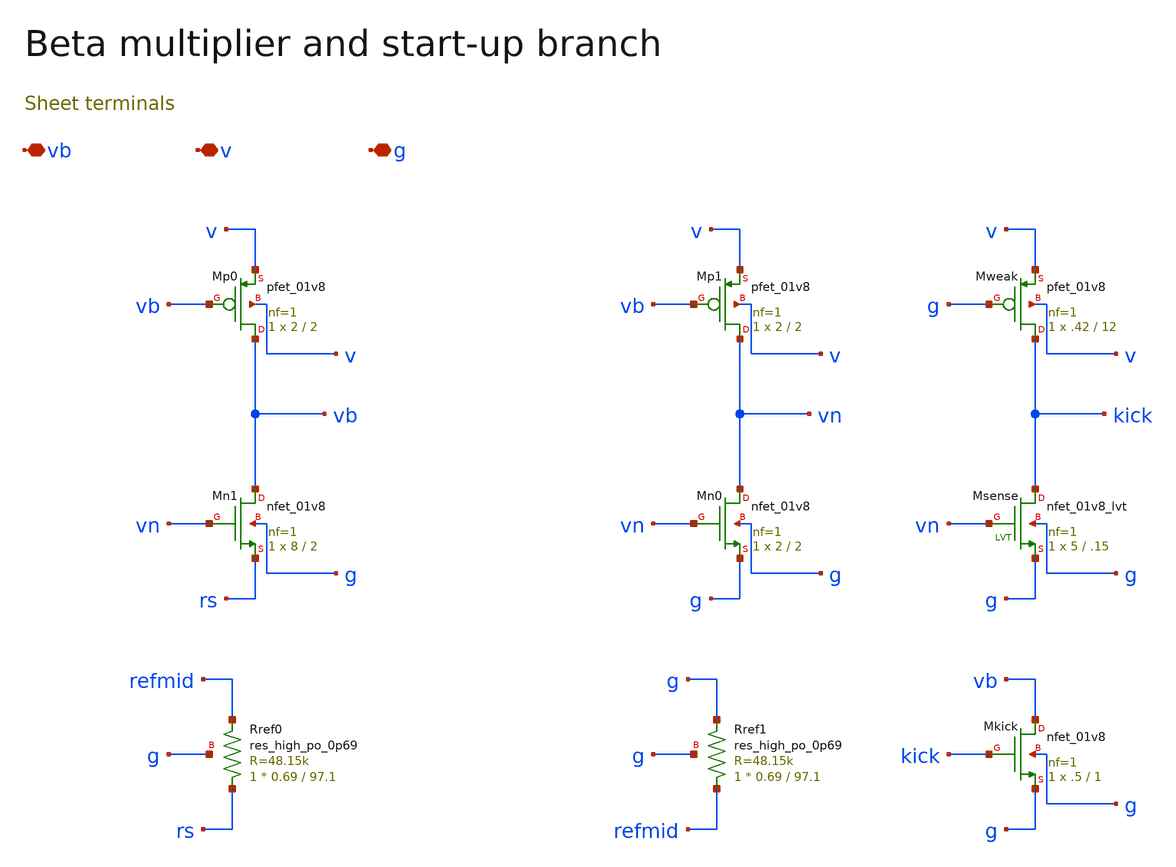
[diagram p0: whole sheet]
** sch_path: review/xschem/beta_ref.sch
**.subckt beta_ref vb v g
*.iopin vb
*.iopin v
*.iopin g
XMp0 vb vb v v sky130_fd_pr__pfet_01v8 L=2 W=2 nf=1 ad='int((nf+1)/2) * W/nf * 0.29' as='int((nf+2)/2) * W/nf * 0.29'
+ pd='2*int((nf+1)/2) * (W/nf + 0.29)' ps='2*int((nf+2)/2) * (W/nf + 0.29)' nrd='0.29 / W' nrs='0.29 / W'
+ sa=0 sb=0 sd=0 mult=1 m=1
XMn0 vn vn g g sky130_fd_pr__nfet_01v8 L=2 W=2 nf=1 ad='int((1 + 1)/2) * 2 / 1 * 0.29' as='int((1 + 2)/2) * 2 / 1 * 0.29'
+ pd='2*int((1 + 1)/2) * (2 / 1 + 0.29)' ps='2*int((1 + 2)/2) * (2 / 1 + 0.29)' nrd='0.29 / 2 ' nrs='0.29 / 2 '
+ sa=0 sb=0 sd=0 mult=1 m=1
XMp1 vn vb v v sky130_fd_pr__pfet_01v8 L=2 W=2 nf=1 ad='int((nf+1)/2) * W/nf * 0.29' as='int((nf+2)/2) * W/nf * 0.29'
+ pd='2*int((nf+1)/2) * (W/nf + 0.29)' ps='2*int((nf+2)/2) * (W/nf + 0.29)' nrd='0.29 / W' nrs='0.29 / W'
+ sa=0 sb=0 sd=0 mult=1 m=1
XMn1 vb vn rs g sky130_fd_pr__nfet_01v8 L=2 W=8 nf=1 ad='int((1 + 1)/2) * 8 / 1 * 0.29' as='int((1 + 2)/2) * 8 / 1 * 0.29'
+ pd='2*int((1 + 1)/2) * (8 / 1 + 0.29)' ps='2*int((1 + 2)/2) * (8 / 1 + 0.29)' nrd='0.29 / 8 ' nrs='0.29 / 8 '
+ sa=0 sb=0 sd=0 mult=1 m=1
XRref0 rs refmid g sky130_fd_pr__res_high_po_0p69 L=97.1 mult=1 m=1
XRref1 refmid g g sky130_fd_pr__res_high_po_0p69 L=97.1 mult=1 m=1
XMweak kick g v v sky130_fd_pr__pfet_01v8 L=12 W=.42 nf=1 ad='int((nf+1)/2) * W/nf * 0.29' as='int((nf+2)/2) * W/nf * 0.29'
+ pd='2*int((nf+1)/2) * (W/nf + 0.29)' ps='2*int((nf+2)/2) * (W/nf + 0.29)' nrd='0.29 / W' nrs='0.29 / W'
+ sa=0 sb=0 sd=0 mult=1 m=1
XMsense kick vn g g sky130_fd_pr__nfet_01v8_lvt L=.15 W=5 nf=1 ad='int((1 + 1)/2) * 5 / 1 * 0.29' as='int((1 + 2)/2) * 5 / 1 * 0.29'
+ pd='2*int((1 + 1)/2) * (5 / 1 + 0.29)' ps='2*int((1 + 2)/2) * (5 / 1 + 0.29)' nrd='0.29 / 5 ' nrs='0.29 / 5 '
+ sa=0 sb=0 sd=0 mult=1 m=1
XMkick vb kick g g sky130_fd_pr__nfet_01v8 L=1 W=.5 nf=1 ad='int((1 + 1)/2) * .5 / 1 * 0.29' as='int((1 + 2)/2) * .5 / 1 * 0.29'
+ pd='2*int((1 + 1)/2) * (.5 / 1 + 0.29)' ps='2*int((1 + 2)/2) * (.5 / 1 + 0.29)' nrd='0.29 / .5 ' nrs='0.29 / .5 '
+ sa=0 sb=0 sd=0 mult=1 m=1
**.ends
.end
